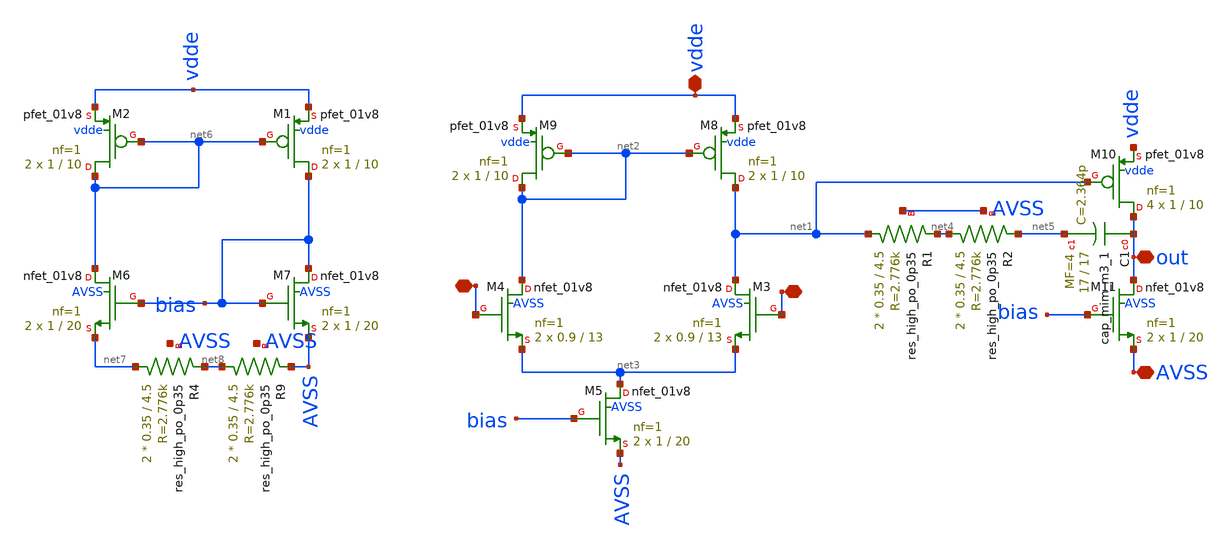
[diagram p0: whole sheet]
** sch_path: xschem/op5.sch
**.subckt op5 AVSS - + vdde out
*.iopin AVSS
*.iopin -
*.iopin +
*.iopin vdde
*.iopin out
XM8 net1 net2 vdde vdde sky130_fd_pr__pfet_01v8 L=10 W=1 nf=1 ad='int((nf+1)/2) * W/nf * 0.29' as='int((nf+2)/2) * W/nf * 0.29'
+ pd='2*int((nf+1)/2) * (W/nf + 0.29)' ps='2*int((nf+2)/2) * (W/nf + 0.29)' nrd='0.29 / W' nrs='0.29 / W'
+ sa=0 sb=0 sd=0 mult=2 m=2
XM9 net2 net2 vdde vdde sky130_fd_pr__pfet_01v8 L=10 W=1 nf=1 ad='int((nf+1)/2) * W/nf * 0.29' as='int((nf+2)/2) * W/nf * 0.29'
+ pd='2*int((nf+1)/2) * (W/nf + 0.29)' ps='2*int((nf+2)/2) * (W/nf + 0.29)' nrd='0.29 / W' nrs='0.29 / W'
+ sa=0 sb=0 sd=0 mult=2 m=2
XM5 net3 bias AVSS AVSS sky130_fd_pr__nfet_01v8 L=20 W=1 nf=1 ad='int((nf+1)/2) * W/nf * 0.29' as='int((nf+2)/2) * W/nf * 0.29'
+ pd='2*int((nf+1)/2) * (W/nf + 0.29)' ps='2*int((nf+2)/2) * (W/nf + 0.29)' nrd='0.29 / W' nrs='0.29 / W'
+ sa=0 sb=0 sd=0 mult=2 m=2
XM10 out net1 vdde vdde sky130_fd_pr__pfet_01v8 L=10 W=1 nf=1 ad='int((nf+1)/2) * W/nf * 0.29' as='int((nf+2)/2) * W/nf * 0.29'
+ pd='2*int((nf+1)/2) * (W/nf + 0.29)' ps='2*int((nf+2)/2) * (W/nf + 0.29)' nrd='0.29 / W' nrs='0.29 / W'
+ sa=0 sb=0 sd=0 mult=4 m=4
XM11 out bias AVSS AVSS sky130_fd_pr__nfet_01v8 L=20 W=1 nf=1 ad='int((nf+1)/2) * W/nf * 0.29' as='int((nf+2)/2) * W/nf * 0.29'
+ pd='2*int((nf+1)/2) * (W/nf + 0.29)' ps='2*int((nf+2)/2) * (W/nf + 0.29)' nrd='0.29 / W' nrs='0.29 / W'
+ sa=0 sb=0 sd=0 mult=2 m=2
XM3 net1 + net3 AVSS sky130_fd_pr__nfet_01v8 L=13 W=0.9 nf=1 ad='int((nf+1)/2) * W/nf * 0.29' as='int((nf+2)/2) * W/nf * 0.29'
+ pd='2*int((nf+1)/2) * (W/nf + 0.29)' ps='2*int((nf+2)/2) * (W/nf + 0.29)' nrd='0.29 / W' nrs='0.29 / W'
+ sa=0 sb=0 sd=0 mult=2 m=2
XM1 bias net6 vdde vdde sky130_fd_pr__pfet_01v8 L=10 W=1 nf=1 ad='int((nf+1)/2) * W/nf * 0.29' as='int((nf+2)/2) * W/nf * 0.29'
+ pd='2*int((nf+1)/2) * (W/nf + 0.29)' ps='2*int((nf+2)/2) * (W/nf + 0.29)' nrd='0.29 / W' nrs='0.29 / W'
+ sa=0 sb=0 sd=0 mult=2 m=2
XM2 net6 net6 vdde vdde sky130_fd_pr__pfet_01v8 L=10 W=1 nf=1 ad='int((nf+1)/2) * W/nf * 0.29' as='int((nf+2)/2) * W/nf * 0.29'
+ pd='2*int((nf+1)/2) * (W/nf + 0.29)' ps='2*int((nf+2)/2) * (W/nf + 0.29)' nrd='0.29 / W' nrs='0.29 / W'
+ sa=0 sb=0 sd=0 mult=2 m=2
XM6 net6 bias net7 AVSS sky130_fd_pr__nfet_01v8 L=20 W=1 nf=1 ad='int((nf+1)/2) * W/nf * 0.29' as='int((nf+2)/2) * W/nf * 0.29'
+ pd='2*int((nf+1)/2) * (W/nf + 0.29)' ps='2*int((nf+2)/2) * (W/nf + 0.29)' nrd='0.29 / W' nrs='0.29 / W'
+ sa=0 sb=0 sd=0 mult=2 m=2
XM7 bias bias AVSS AVSS sky130_fd_pr__nfet_01v8 L=20 W=1 nf=1 ad='int((nf+1)/2) * W/nf * 0.29' as='int((nf+2)/2) * W/nf * 0.29'
+ pd='2*int((nf+1)/2) * (W/nf + 0.29)' ps='2*int((nf+2)/2) * (W/nf + 0.29)' nrd='0.29 / W' nrs='0.29 / W'
+ sa=0 sb=0 sd=0 mult=2 m=2
XR4 net7 net8 AVSS sky130_fd_pr__res_high_po_0p35 L=4.5 mult=2 m=2
XM4 net2 - net3 AVSS sky130_fd_pr__nfet_01v8 L=13 W=0.9 nf=1 ad='int((nf+1)/2) * W/nf * 0.29' as='int((nf+2)/2) * W/nf * 0.29'
+ pd='2*int((nf+1)/2) * (W/nf + 0.29)' ps='2*int((nf+2)/2) * (W/nf + 0.29)' nrd='0.29 / W' nrs='0.29 / W'
+ sa=0 sb=0 sd=0 mult=2 m=2
XR1 net1 net4 AVSS sky130_fd_pr__res_high_po_0p35 L=4.5 mult=2 m=2
XR2 net4 net5 AVSS sky130_fd_pr__res_high_po_0p35 L=4.5 mult=2 m=2
XC1 out net5 sky130_fd_pr__cap_mim_m3_1 W=17 L=17 MF=4 m=4
XR9 net8 AVSS AVSS sky130_fd_pr__res_high_po_0p35 L=4.5 mult=2 m=2
**.ends
.end
